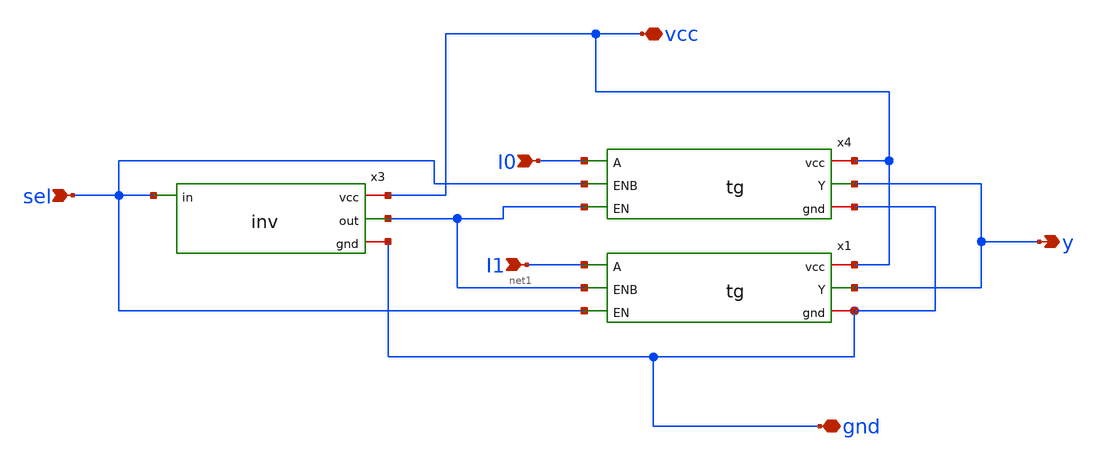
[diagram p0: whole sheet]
** sch_path: designs/schematics/mux2x1/mux.sch
**.subckt mux I0 I1 y vcc gnd sel
*.ipin I0
*.ipin I1
*.opin y
*.iopin vcc
*.iopin gnd
*.ipin sel
x3 vcc sel net1 gnd inv
x4 vcc I0 sel y gnd net1 tg
x1 vcc I1 net1 y gnd sel tg
**.ends

* expanding   symbol:  voidwalkers-scandff-gf180mcu/designs/schematics/mux2x1/inv.sym # of pins=4
** sym_path: designs/schematics/mux2x1/inv.sym
** sch_path: designs/schematics/mux2x1/inv.sch
.subckt inv vcc in out gnd
*.ipin in
*.opin out
*.iopin vcc
*.iopin gnd
XM2 out in vcc vcc pfet_03v3 L=0.28u W=0.22u nf=1 ad='int((nf+1)/2) * W/nf * 0.18u' as='int((nf+2)/2) * W/nf * 0.18u'
+ pd='2*int((nf+1)/2) * (W/nf + 0.18u)' ps='2*int((nf+2)/2) * (W/nf + 0.18u)' nrd='0.18u / W' nrs='0.18u / W'
+ sa=0 sb=0 sd=0 m=1
XM1 out in gnd gnd nfet_03v3 L=0.28u W=0.22u nf=1 ad='int((nf+1)/2) * W/nf * 0.18u' as='int((nf+2)/2) * W/nf * 0.18u'
+ pd='2*int((nf+1)/2) * (W/nf + 0.18u)' ps='2*int((nf+2)/2) * (W/nf + 0.18u)' nrd='0.18u / W' nrs='0.18u / W'
+ sa=0 sb=0 sd=0 m=1
.ends


* expanding   symbol:  voidwalkers-scandff-gf180mcu/designs/schematics/mux2x1/tg.sym # of pins=6
** sym_path: designs/schematics/mux2x1/tg.sym
** sch_path: designs/schematics/mux2x1/tg.sch
.subckt tg vcc A ENB Y gnd EN
*.ipin A
*.ipin EN
*.opin Y
*.ipin ENB
*.iopin gnd
*.iopin vcc
XM1 Y EN A gnd nfet_03v3 L=0.28u W=0.22u nf=1 ad='int((nf+1)/2) * W/nf * 0.18u' as='int((nf+2)/2) * W/nf * 0.18u'
+ pd='2*int((nf+1)/2) * (W/nf + 0.18u)' ps='2*int((nf+2)/2) * (W/nf + 0.18u)' nrd='0.18u / W' nrs='0.18u / W'
+ sa=0 sb=0 sd=0 m=1
XM3 Y ENB A vcc pfet_03v3 L=0.28u W=0.22u nf=1 ad='int((nf+1)/2) * W/nf * 0.18u' as='int((nf+2)/2) * W/nf * 0.18u'
+ pd='2*int((nf+1)/2) * (W/nf + 0.18u)' ps='2*int((nf+2)/2) * (W/nf + 0.18u)' nrd='0.18u / W' nrs='0.18u / W'
+ sa=0 sb=0 sd=0 m=1
.ends

.end
